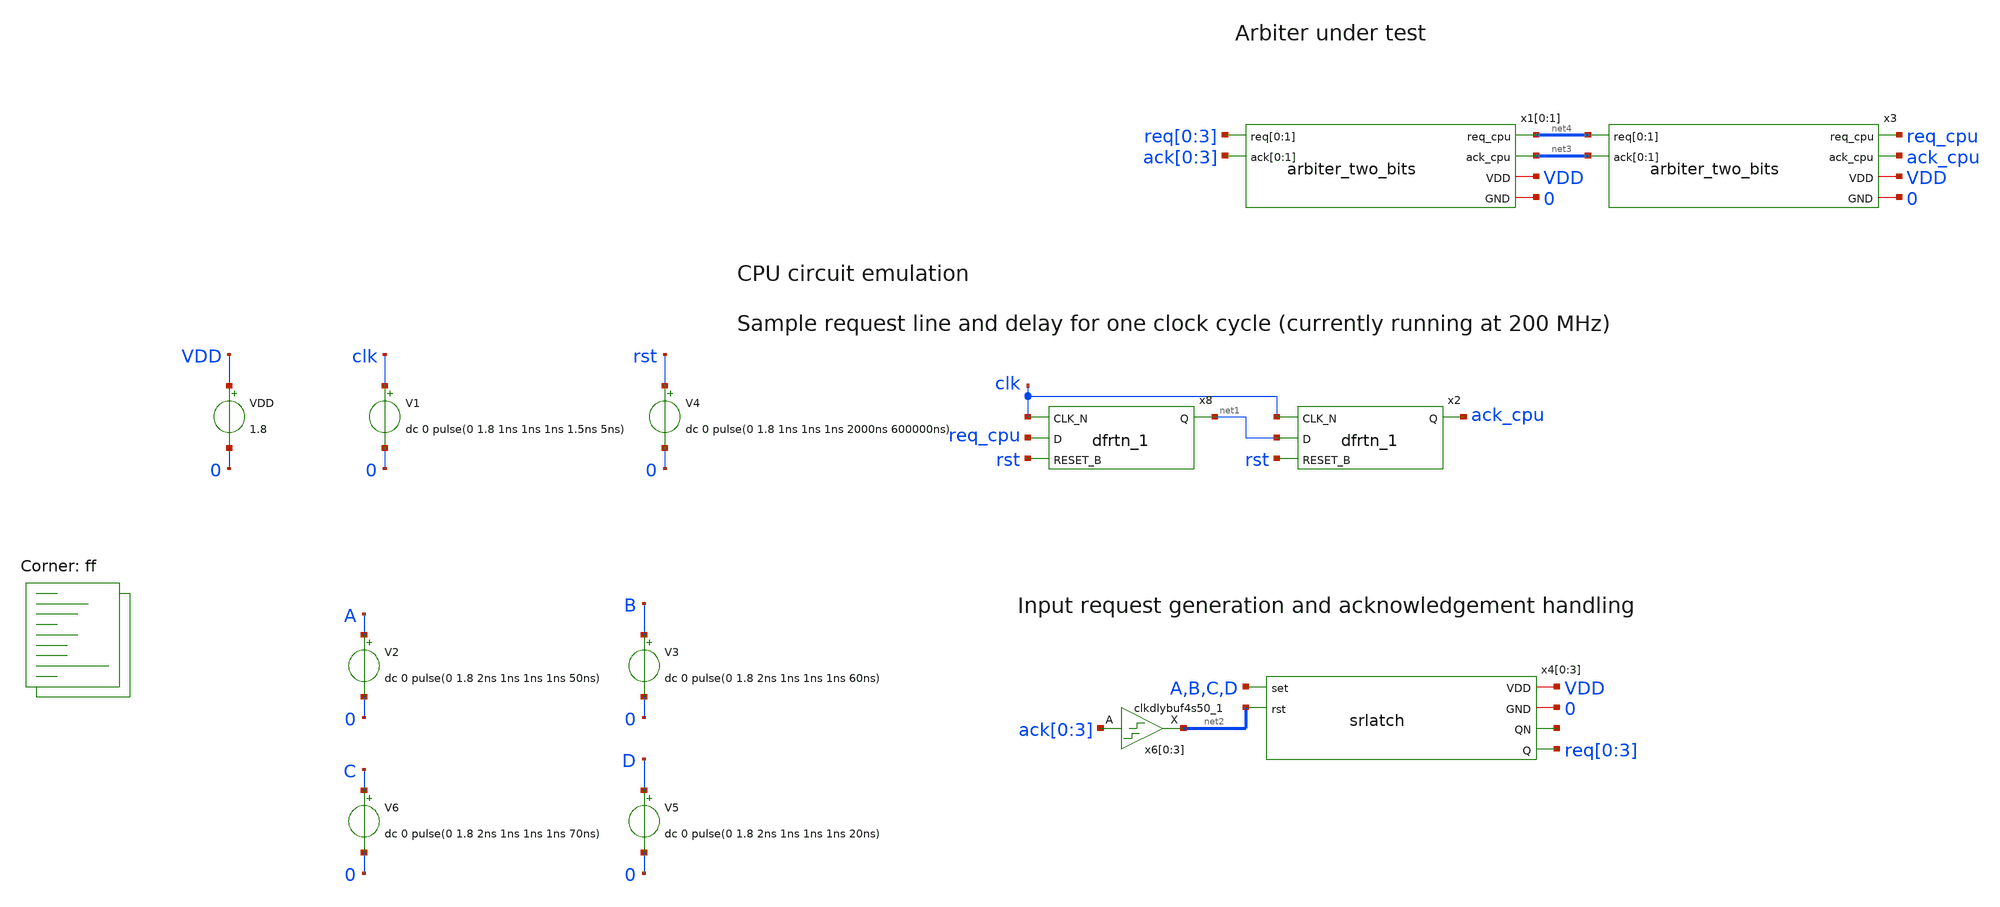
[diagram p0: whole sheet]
** sch_path: design/xschem/arbiter_four_bits_tb.sch
**.subckt arbiter_four_bits_tb
V3 B 0 dc 0 pulse(0 1.8 2ns 1ns 1ns 1ns 60ns)
V2 A 0 dc 0 pulse(0 1.8 2ns 1ns 1ns 1ns 50ns)
V1 clk 0 dc 0 pulse(0 1.8 1ns 1ns 1ns 1.5ns 5ns)
x4[0] VDD 0 A net5[3] req[0] net2[3] srlatch
x4[1] VDD 0 B net5[2] req[1] net2[2] srlatch
x4[2] VDD 0 C net5[1] req[2] net2[1] srlatch
x4[3] VDD 0 D net5[0] req[3] net2[0] srlatch
x6[0] ack[0] 0 0 VDD VDD net2[3] sky130_fd_sc_hd__clkdlybuf4s50_1
x6[1] ack[1] 0 0 VDD VDD net2[2] sky130_fd_sc_hd__clkdlybuf4s50_1
x6[2] ack[2] 0 0 VDD VDD net2[1] sky130_fd_sc_hd__clkdlybuf4s50_1
x6[3] ack[3] 0 0 VDD VDD net2[0] sky130_fd_sc_hd__clkdlybuf4s50_1
x8 clk req_cpu rst 0 0 VDD VDD net1 sky130_fd_sc_hd__dfrtn_1
x2 clk net1 rst 0 0 VDD VDD ack_cpu sky130_fd_sc_hd__dfrtn_1
V4 rst 0 dc 0 pulse(0 1.8 1ns 1ns 1ns 2000ns 600000ns)
x3 net4[1] net4[0] ack_cpu net3[1] net3[0] req_cpu VDD 0 arbiter_two_bits
x1[0] req[0] req[1] net3[1] ack[0] ack[1] net4[1] VDD 0 arbiter_two_bits
x1[1] req[2] req[3] net3[0] ack[2] ack[3] net4[0] VDD 0 arbiter_two_bits
V5 D 0 dc 0 pulse(0 1.8 2ns 1ns 1ns 1ns 20ns)
V6 C 0 dc 0 pulse(0 1.8 2ns 1ns 1ns 1ns 70ns)
VDD VDD 0 1.8
**** begin user architecture code
.lib $::SKYWATER_MODELS/sky130.lib.spice ff


* Standard cell simulation files
.include $::SKYWATER_STDCELLS/sky130_fd_sc_hd.spice







.save all
.control
 tran 0.02ns 200ns
 write arbiter_four_bits_tb.raw
 quit 0
.endc



**** end user architecture code
**.ends

* expanding   symbol:  srlatch.sym # of pins=6
** sym_path: design/xschem/srlatch.sym
** sch_path: design/xschem/srlatch.sch
.subckt srlatch VDD GND set QN Q rst
*.ipin set
*.ipin rst
*.opin Q
*.opin QN
*.iopin VDD
*.iopin GND
x1 set Q GND GND VDD VDD QN sky130_fd_sc_hd__nor2_1
x2 QN rst GND GND VDD VDD Q sky130_fd_sc_hd__nor2_1
.ends


* expanding   symbol:  arbiter_two_bits.sym # of pins=6
** sym_path: design/xschem/arbiter_two_bits.sym
** sch_path: design/xschem/arbiter_two_bits.sch
.subckt arbiter_two_bits req[0] req[1] ack_cpu ack[0] ack[1] req_cpu VDD GND
*.ipin req[0],req[1]
*.opin ack[0],ack[1]
*.ipin ack_cpu
*.opin req_cpu
*.iopin VDD
*.iopin GND
x1 ack[1] ack[0] ack_cpu req_cpu req[0] req[1] VDD GND arbiter_cell_two_bits_fc
.ends


* expanding   symbol:  arbiter_cell_two_bits_fc.sym # of pins=8
** sym_path: design/xschem/arbiter_cell_two_bits_fc.sym
** sch_path: design/xschem/arbiter_cell_two_bits_fc.sch
.subckt arbiter_cell_two_bits_fc g1 g0 gc rc r0 r1 VDD GND
*.ipin r1
*.ipin r0
*.opin g0
*.opin g1
*.opin rc
*.ipin gc
*.iopin GND
*.iopin VDD
x1 net6 net5 GND GND VDD VDD net7 sky130_fd_sc_hd__nand2_1
x2 r0 gc GND GND VDD VDD net4 sky130_fd_sc_hd__or2_1
x3 net3 net1 GND GND VDD VDD g0 sky130_fd_sc_hd__nor2_1
x4 net6 net6 net6 net6 GND GND VDD VDD net3 sky130_fd_sc_hd__or4_1
x5 gc GND GND VDD VDD net1 sky130_fd_sc_hd__inv_1
x6 gc r1 GND GND VDD VDD net5 sky130_fd_sc_hd__or2_1
x7 net4 net7 GND GND VDD VDD net6 sky130_fd_sc_hd__nand2_1
x8 net7 net7 net7 net7 GND GND VDD VDD net2 sky130_fd_sc_hd__or4_1
x9 net1 net2 GND GND VDD VDD g1 sky130_fd_sc_hd__nor2_1
x10 net2 r0 GND GND VDD VDD net8 sky130_fd_sc_hd__nand2_1
x11 net3 r1 GND GND VDD VDD net9 sky130_fd_sc_hd__nand2_1
x12 net8 net9 GND GND VDD VDD rc sky130_fd_sc_hd__nand2_1
.ends

.end
